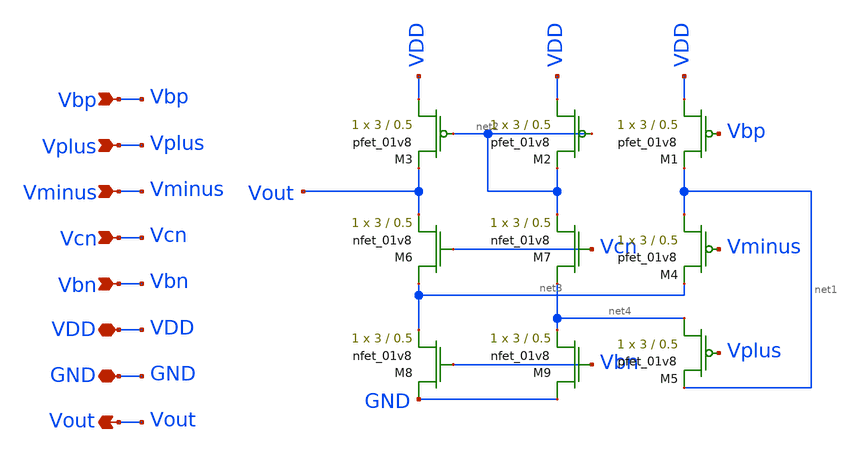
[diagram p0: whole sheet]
** sch_path: final/LDS/cascoded_opamp_pmos_LDS.sch
**.subckt cascoded_opamp_pmos_LDS Vbp Vplus Vminus Vcn Vbn VDD GND Vout
*.ipin Vbp
*.ipin Vplus
*.ipin Vminus
*.ipin Vcn
*.ipin Vbn
*.iopin VDD
*.iopin GND
*.opin Vout
XM1 VDD Vbp net1 VDD sky130_fd_pr__pfet_01v8 L=0.5 W=3 nf=1 ad='int((nf+1)/2) * W/nf * 0.29' as='int((nf+2)/2) * W/nf * 0.29'
+ pd='2*int((nf+1)/2) * (W/nf + 0.29)' ps='2*int((nf+2)/2) * (W/nf + 0.29)' nrd='0.29 / W' nrs='0.29 / W'
+ sa=0 sb=0 sd=0 mult=1 m=1
XM8 GND Vbn net3 GND sky130_fd_pr__nfet_01v8 L=0.5 W=3 nf=1 ad='int((nf+1)/2) * W/nf * 0.29' as='int((nf+2)/2) * W/nf * 0.29'
+ pd='2*int((nf+1)/2) * (W/nf + 0.29)' ps='2*int((nf+2)/2) * (W/nf + 0.29)' nrd='0.29 / W' nrs='0.29 / W'
+ sa=0 sb=0 sd=0 mult=1 m=1
XM2 VDD net2 net2 VDD sky130_fd_pr__pfet_01v8 L=0.5 W=3 nf=1 ad='int((nf+1)/2) * W/nf * 0.29' as='int((nf+2)/2) * W/nf * 0.29'
+ pd='2*int((nf+1)/2) * (W/nf + 0.29)' ps='2*int((nf+2)/2) * (W/nf + 0.29)' nrd='0.29 / W' nrs='0.29 / W'
+ sa=0 sb=0 sd=0 mult=1 m=1
XM3 VDD net2 Vout VDD sky130_fd_pr__pfet_01v8 L=0.5 W=3 nf=1 ad='int((nf+1)/2) * W/nf * 0.29' as='int((nf+2)/2) * W/nf * 0.29'
+ pd='2*int((nf+1)/2) * (W/nf + 0.29)' ps='2*int((nf+2)/2) * (W/nf + 0.29)' nrd='0.29 / W' nrs='0.29 / W'
+ sa=0 sb=0 sd=0 mult=1 m=1
XM4 net1 Vminus net3 VDD sky130_fd_pr__pfet_01v8 L=0.5 W=3 nf=1 ad='int((nf+1)/2) * W/nf * 0.29' as='int((nf+2)/2) * W/nf * 0.29'
+ pd='2*int((nf+1)/2) * (W/nf + 0.29)' ps='2*int((nf+2)/2) * (W/nf + 0.29)' nrd='0.29 / W' nrs='0.29 / W'
+ sa=0 sb=0 sd=0 mult=1 m=1
XM5 net4 Vplus net1 VDD sky130_fd_pr__pfet_01v8 L=0.5 W=3 nf=1 ad='int((nf+1)/2) * W/nf * 0.29' as='int((nf+2)/2) * W/nf * 0.29'
+ pd='2*int((nf+1)/2) * (W/nf + 0.29)' ps='2*int((nf+2)/2) * (W/nf + 0.29)' nrd='0.29 / W' nrs='0.29 / W'
+ sa=0 sb=0 sd=0 mult=1 m=1
XM6 net3 Vcn Vout GND sky130_fd_pr__nfet_01v8 L=0.5 W=3 nf=1 ad='int((nf+1)/2) * W/nf * 0.29' as='int((nf+2)/2) * W/nf * 0.29'
+ pd='2*int((nf+1)/2) * (W/nf + 0.29)' ps='2*int((nf+2)/2) * (W/nf + 0.29)' nrd='0.29 / W' nrs='0.29 / W'
+ sa=0 sb=0 sd=0 mult=1 m=1
XM7 net4 Vcn net2 GND sky130_fd_pr__nfet_01v8 L=0.5 W=3 nf=1 ad='int((nf+1)/2) * W/nf * 0.29' as='int((nf+2)/2) * W/nf * 0.29'
+ pd='2*int((nf+1)/2) * (W/nf + 0.29)' ps='2*int((nf+2)/2) * (W/nf + 0.29)' nrd='0.29 / W' nrs='0.29 / W'
+ sa=0 sb=0 sd=0 mult=1 m=1
XM9 GND Vbn net4 GND sky130_fd_pr__nfet_01v8 L=0.5 W=3 nf=1 ad='int((nf+1)/2) * W/nf * 0.29' as='int((nf+2)/2) * W/nf * 0.29'
+ pd='2*int((nf+1)/2) * (W/nf + 0.29)' ps='2*int((nf+2)/2) * (W/nf + 0.29)' nrd='0.29 / W' nrs='0.29 / W'
+ sa=0 sb=0 sd=0 mult=1 m=1
**.ends
.end
